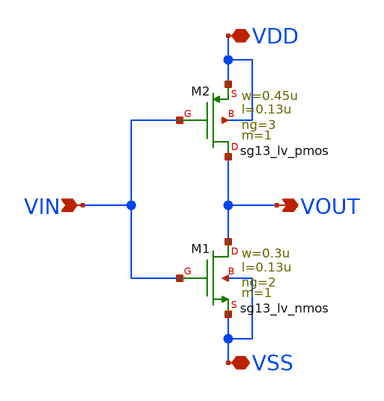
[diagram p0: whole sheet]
** sch_path: CDR4176-main/schematic/xschem/inv_PI/inv_PI.sch
**.subckt inv_PI VDD VSS VOUT VIN
*.iopin VDD
*.iopin VSS
*.opin VOUT
*.ipin VIN
XM2 VOUT VIN VDD VDD sg13_lv_pmos w=0.45u l=0.13u ng=3 m=1 mm_ok=1
XM1 VOUT VIN VSS VSS sg13_lv_nmos w=0.3u l=0.13u ng=2 m=1 mm_ok=1
**.ends
.end
